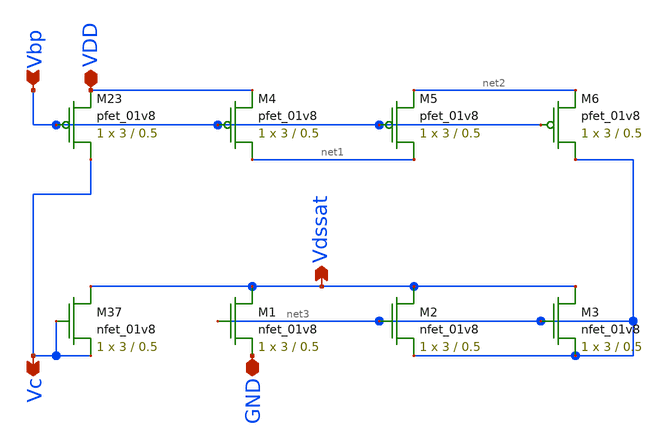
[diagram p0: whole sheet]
** sch_path: final/LDS/cascode_bias_lds.sch
**.subckt cascode_bias_lds GND Vc VDD Vbp Vdssat
*.iopin GND
*.opin Vc
*.iopin VDD
*.ipin Vbp
*.opin Vdssat
XM23 Vc Vbp VDD VDD sky130_fd_pr__pfet_01v8 L=0.5 W=3 nf=1 ad='int((nf+1)/2) * W/nf * 0.29' as='int((nf+2)/2) * W/nf * 0.29'
+ pd='2*int((nf+1)/2) * (W/nf + 0.29)' ps='2*int((nf+2)/2) * (W/nf + 0.29)' nrd='0.29 / W' nrs='0.29 / W'
+ sa=0 sb=0 sd=0 mult=1 m=1
XM37 Vdssat Vc Vc GND sky130_fd_pr__nfet_01v8 L=0.5 W=3 nf=1 ad='int((nf+1)/2) * W/nf * 0.29' as='int((nf+2)/2) * W/nf * 0.29'
+ pd='2*int((nf+1)/2) * (W/nf + 0.29)' ps='2*int((nf+2)/2) * (W/nf + 0.29)' nrd='0.29 / W' nrs='0.29 / W'
+ sa=0 sb=0 sd=0 mult=1 m=1
XM1 Vdssat net3 GND GND sky130_fd_pr__nfet_01v8 L=0.5 W=3 nf=1 ad='int((nf+1)/2) * W/nf * 0.29' as='int((nf+2)/2) * W/nf * 0.29'
+ pd='2*int((nf+1)/2) * (W/nf + 0.29)' ps='2*int((nf+2)/2) * (W/nf + 0.29)' nrd='0.29 / W' nrs='0.29 / W'
+ sa=0 sb=0 sd=0 mult=1 m=1
XM2 Vdssat net3 net3 GND sky130_fd_pr__nfet_01v8 L=0.5 W=3 nf=1 ad='int((nf+1)/2) * W/nf * 0.29' as='int((nf+2)/2) * W/nf * 0.29'
+ pd='2*int((nf+1)/2) * (W/nf + 0.29)' ps='2*int((nf+2)/2) * (W/nf + 0.29)' nrd='0.29 / W' nrs='0.29 / W'
+ sa=0 sb=0 sd=0 mult=1 m=1
XM3 Vdssat net3 net3 GND sky130_fd_pr__nfet_01v8 L=0.5 W=3 nf=1 ad='int((nf+1)/2) * W/nf * 0.29' as='int((nf+2)/2) * W/nf * 0.29'
+ pd='2*int((nf+1)/2) * (W/nf + 0.29)' ps='2*int((nf+2)/2) * (W/nf + 0.29)' nrd='0.29 / W' nrs='0.29 / W'
+ sa=0 sb=0 sd=0 mult=1 m=1
XM4 net1 Vbp VDD VDD sky130_fd_pr__pfet_01v8 L=0.5 W=3 nf=1 ad='int((nf+1)/2) * W/nf * 0.29' as='int((nf+2)/2) * W/nf * 0.29'
+ pd='2*int((nf+1)/2) * (W/nf + 0.29)' ps='2*int((nf+2)/2) * (W/nf + 0.29)' nrd='0.29 / W' nrs='0.29 / W'
+ sa=0 sb=0 sd=0 mult=1 m=1
XM5 net1 Vbp net2 VDD sky130_fd_pr__pfet_01v8 L=0.5 W=3 nf=1 ad='int((nf+1)/2) * W/nf * 0.29' as='int((nf+2)/2) * W/nf * 0.29'
+ pd='2*int((nf+1)/2) * (W/nf + 0.29)' ps='2*int((nf+2)/2) * (W/nf + 0.29)' nrd='0.29 / W' nrs='0.29 / W'
+ sa=0 sb=0 sd=0 mult=1 m=1
XM6 net3 Vbp net2 VDD sky130_fd_pr__pfet_01v8 L=0.5 W=3 nf=1 ad='int((nf+1)/2) * W/nf * 0.29' as='int((nf+2)/2) * W/nf * 0.29'
+ pd='2*int((nf+1)/2) * (W/nf + 0.29)' ps='2*int((nf+2)/2) * (W/nf + 0.29)' nrd='0.29 / W' nrs='0.29 / W'
+ sa=0 sb=0 sd=0 mult=1 m=1
**.ends
.end
